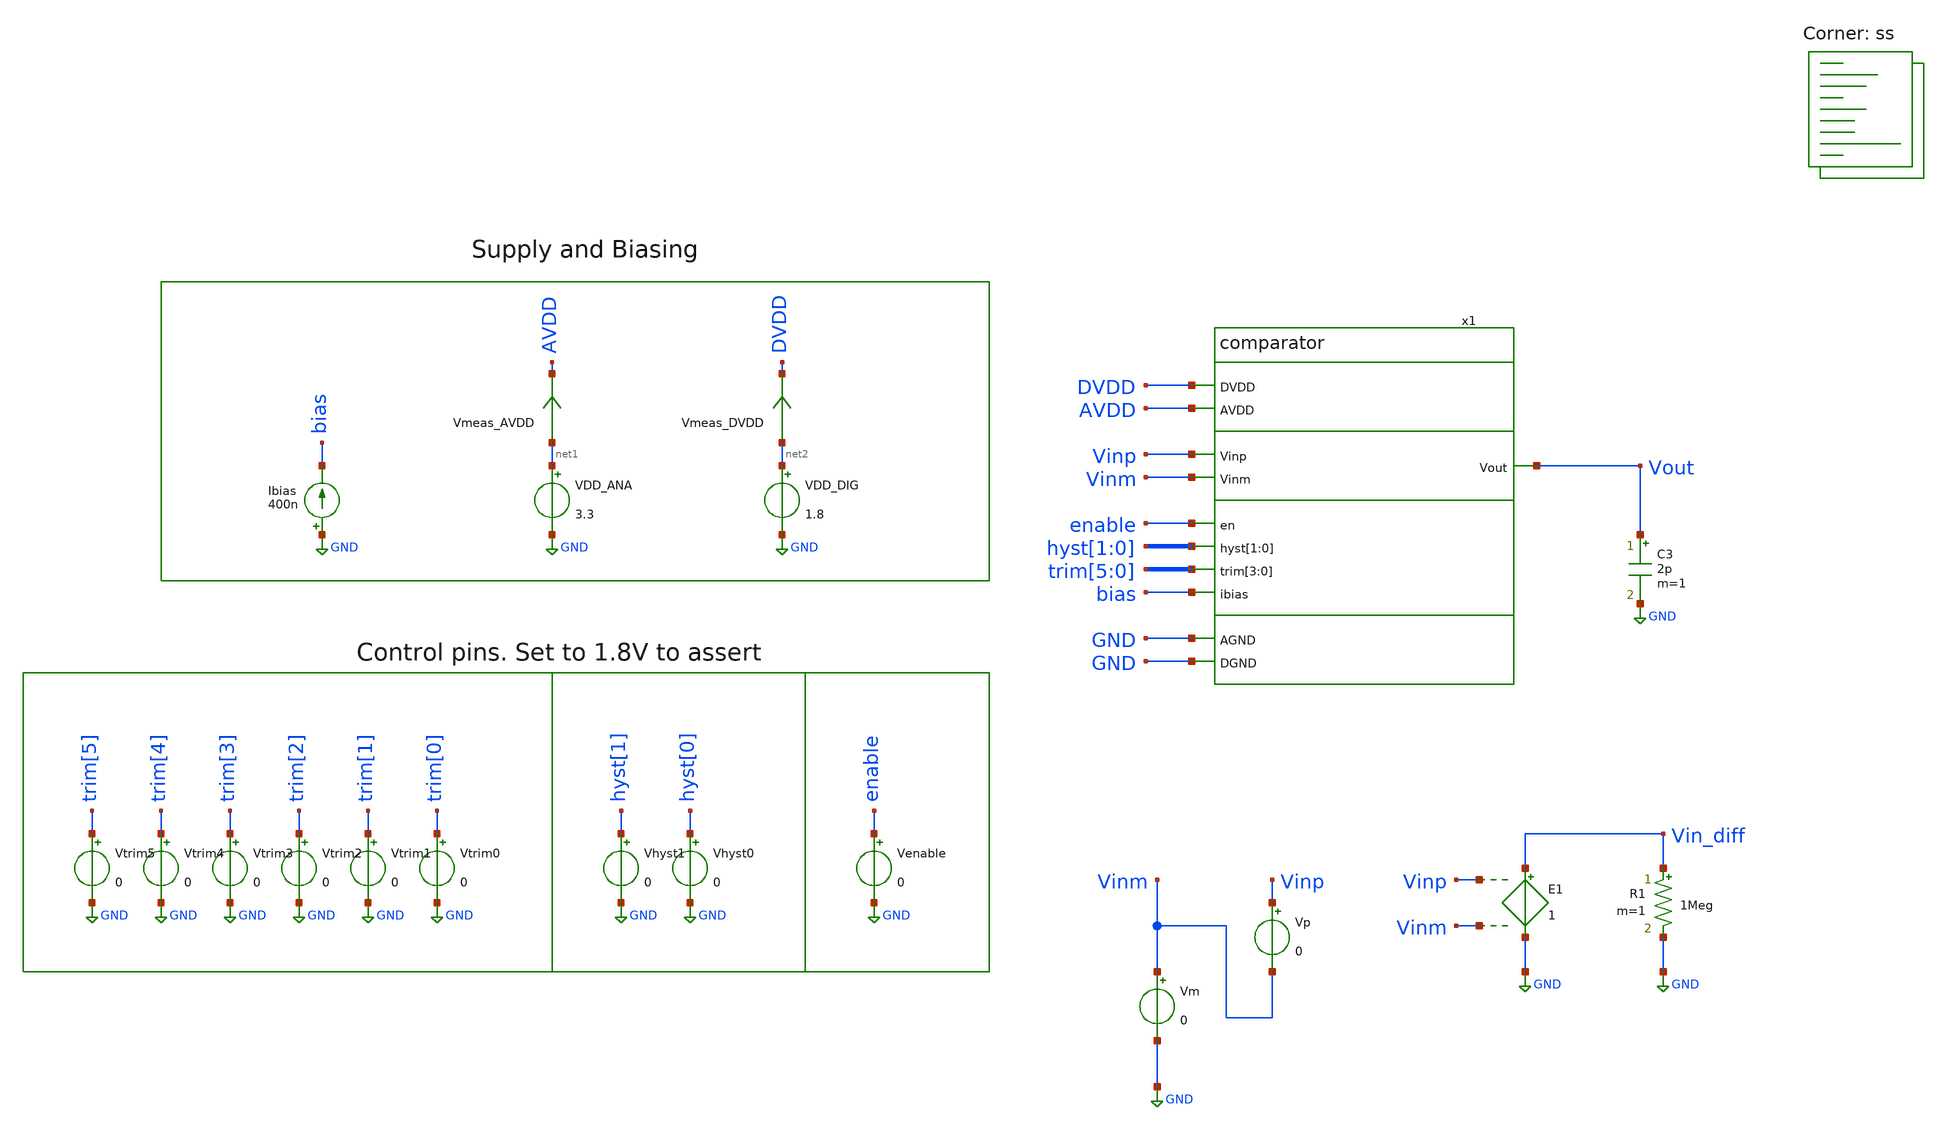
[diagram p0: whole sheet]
** sch_path: xschem/tb_comparator_consumption_disabled.sch
**.subckt tb_comparator_consumption_disabled
Vp Vinp Vinm 0
VDD_ANA net1 GND 3.3
VDD_DIG net2 GND 1.8
Ibias GND bias 400n
C3 Vout GND 2p m=1
Vm Vinm GND 0
Vmeas_AVDD net1 AVDD 0
.save i(vmeas_avdd)
Vmeas_DVDD net2 DVDD 0
.save i(vmeas_dvdd)
E1 Vin_diff GND Vinp Vinm 1
Vtrim3 trim[3] GND 0
Vtrim2 trim[2] GND 0
Vtrim1 trim[1] GND 0
Vtrim0 trim[0] GND 0
Vhyst1 hyst[1] GND 0
Vhyst0 hyst[0] GND 0
Venable enable GND 0
Vtrim5 trim[5] GND 0
Vtrim4 trim[4] GND 0
R1 Vin_diff GND 1Meg m=1
x1 DVDD AVDD GND GND Vinp Vout Vinm enable hyst[1] hyst[0] trim[5] trim[4] trim[3] trim[2] bias
+ comparator
**** begin user architecture code
.lib $::SKYWATER_MODELS/sky130.lib.spice ss


.save all
.tran 1u 1m 500u

.control
let vec=unitvec(1)
foreach temp_val -40 27 85
   set temp=$temp_val
   foreach vdd_ana_val 2.95 3.3 5.5
      alter VDD_ANA $vdd_ana_val
      foreach vm_val 0 {$vdd_ana_val/4} {$vdd_ana_val/2} {$vdd_ana_val*3/4} {-0.1+$vdd_ana_val}
         alter Vm $vm_val
         foreach ibias_val 400n
            alter Ibias $ibias_val
            nodeset v(x1.trim5_hv)=0 v(x1.trim4_hv)=0 v(x1.trim3_hv)=0 v(x1.trim2_hv)=0
+ v(x1.trim1_hv)=0 v(x1.trim0_hv)=0 v(x1.en_hv)=0 v(x1.hyst1_hv)=0 v(x1.hyst0_hv)=0
            run
            set filetype=ascii
            set appendwrite
            set wr_singlescale
            setscale vec
            wrdata results_current_cons_disabled.out mean(i(vdd_ana)) mean(i(vdd_dig))
            print mean(i(vdd_ana))
            print mean(i(vdd_dig))
         end
      end
   end
end
*plot tran1.i(vdd_ana) tran2.i(vdd_ana) tran6.i(vdd_ana)
.endc


**** end user architecture code
**.ends
.GLOBAL GND
.end
